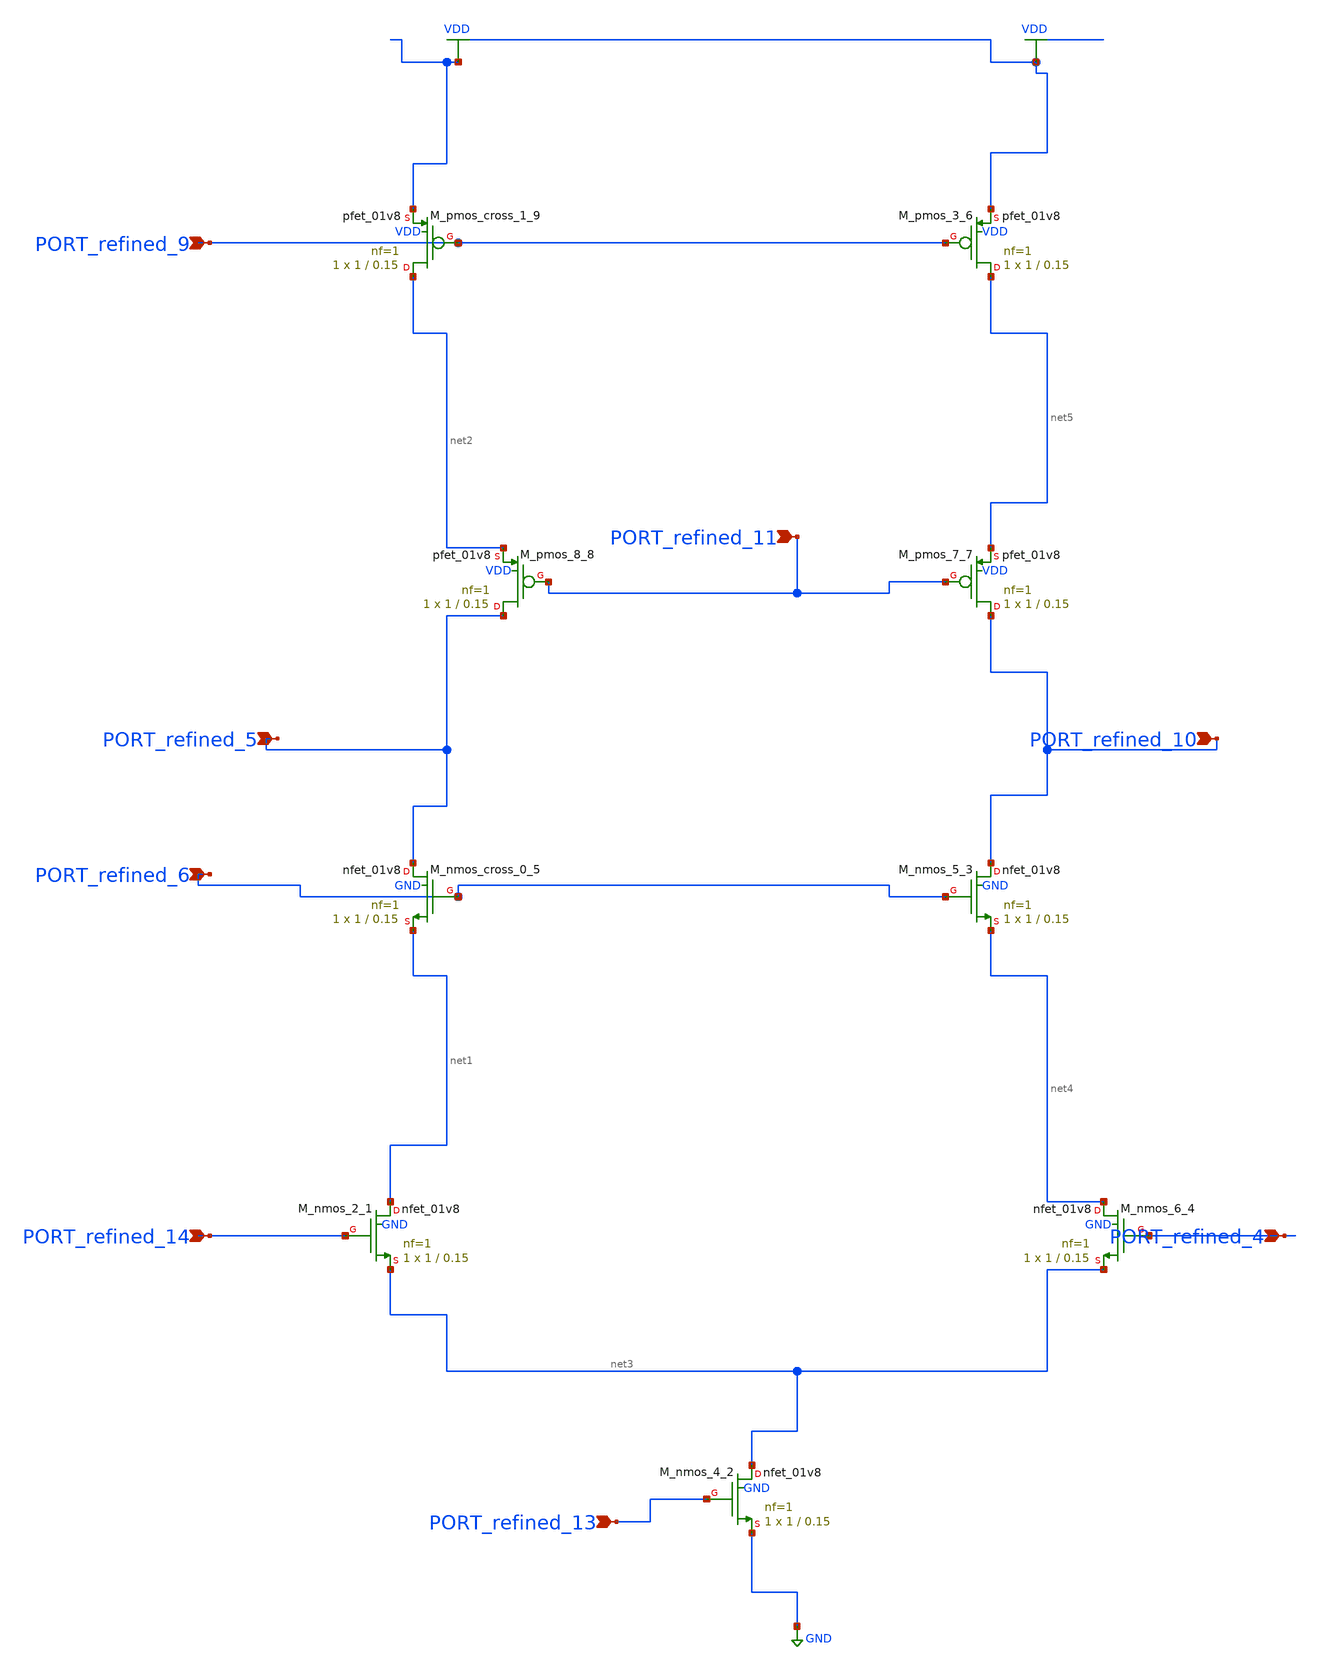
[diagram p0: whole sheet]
** sch_path: schematics/AMSNet/753.sch
**.subckt 753 PORT_refined_13 PORT_refined_4 PORT_refined_6 PORT_refined_11 PORT_refined_10
*+ PORT_refined_14 PORT_refined_5 PORT_refined_9
*.ipin PORT_refined_13
*.ipin PORT_refined_4
*.ipin PORT_refined_6
*.ipin PORT_refined_11
*.ipin PORT_refined_10
*.ipin PORT_refined_14
*.ipin PORT_refined_5
*.ipin PORT_refined_9
XM_nmos_2_1 net1 PORT_refined_14 net3 GND sky130_fd_pr__nfet_01v8 L=0.15 W=1 nf=1 ad='int((1 + 1)/2) * 1 / 1 * 0.29'
+ as='int((1 + 2)/2) * 1 / 1 * 0.29' pd='2*int((1 + 1)/2) * (1 / 1 + 0.29)' ps='2*int((1 + 2)/2) * (1 / 1 + 0.29)'
+ nrd='0.29 / 1 ' nrs='0.29 / 1 ' sa=0 sb=0 sd=0 mult=1 m=1
XM_nmos_4_2 net3 PORT_refined_13 GND GND sky130_fd_pr__nfet_01v8 L=0.15 W=1 nf=1 ad='int((1 + 1)/2) * 1 / 1 * 0.29'
+ as='int((1 + 2)/2) * 1 / 1 * 0.29' pd='2*int((1 + 1)/2) * (1 / 1 + 0.29)' ps='2*int((1 + 2)/2) * (1 / 1 + 0.29)'
+ nrd='0.29 / 1 ' nrs='0.29 / 1 ' sa=0 sb=0 sd=0 mult=1 m=1
XM_nmos_5_3 PORT_refined_10 PORT_refined_6 net4 GND sky130_fd_pr__nfet_01v8 L=0.15 W=1 nf=1 ad='int((1 + 1)/2) * 1 / 1 * 0.29'
+ as='int((1 + 2)/2) * 1 / 1 * 0.29' pd='2*int((1 + 1)/2) * (1 / 1 + 0.29)' ps='2*int((1 + 2)/2) * (1 / 1 + 0.29)'
+ nrd='0.29 / 1 ' nrs='0.29 / 1 ' sa=0 sb=0 sd=0 mult=1 m=1
XM_nmos_6_4 net4 PORT_refined_4 net3 GND sky130_fd_pr__nfet_01v8 L=0.15 W=1 nf=1 ad='int((1 + 1)/2) * 1 / 1 * 0.29'
+ as='int((1 + 2)/2) * 1 / 1 * 0.29' pd='2*int((1 + 1)/2) * (1 / 1 + 0.29)' ps='2*int((1 + 2)/2) * (1 / 1 + 0.29)'
+ nrd='0.29 / 1 ' nrs='0.29 / 1 ' sa=0 sb=0 sd=0 mult=1 m=1
XM_nmos_cross_0_5 PORT_refined_5 PORT_refined_6 net1 GND sky130_fd_pr__nfet_01v8 L=0.15 W=1 nf=1 ad='int((1 + 1)/2) * 1 / 1 * 0.29'
+ as='int((1 + 2)/2) * 1 / 1 * 0.29' pd='2*int((1 + 1)/2) * (1 / 1 + 0.29)' ps='2*int((1 + 2)/2) * (1 / 1 + 0.29)'
+ nrd='0.29 / 1 ' nrs='0.29 / 1 ' sa=0 sb=0 sd=0 mult=1 m=1
XM_pmos_3_6 net5 PORT_refined_9 VDD VDD sky130_fd_pr__pfet_01v8 L=0.15 W=1 nf=1 ad='int((1 + 1)/2) * 1 / 1 * 0.29'
+ as='int((1 + 2)/2) * 1 / 1 * 0.29' pd='2*int((1 + 1)/2) * (1 / 1 + 0.29)' ps='2*int((1 + 2)/2) * (1 / 1 + 0.29)'
+ nrd='0.29 / 1 ' nrs='0.29 / 1 ' sa=0 sb=0 sd=0 mult=1 m=1
XM_pmos_7_7 PORT_refined_10 PORT_refined_11 net5 VDD sky130_fd_pr__pfet_01v8 L=0.15 W=1 nf=1 ad='int((1 + 1)/2) * 1 / 1 * 0.29'
+ as='int((1 + 2)/2) * 1 / 1 * 0.29' pd='2*int((1 + 1)/2) * (1 / 1 + 0.29)' ps='2*int((1 + 2)/2) * (1 / 1 + 0.29)'
+ nrd='0.29 / 1 ' nrs='0.29 / 1 ' sa=0 sb=0 sd=0 mult=1 m=1
XM_pmos_8_8 PORT_refined_5 PORT_refined_11 net2 VDD sky130_fd_pr__pfet_01v8 L=0.15 W=1 nf=1 ad='int((1 + 1)/2) * 1 / 1 * 0.29'
+ as='int((1 + 2)/2) * 1 / 1 * 0.29' pd='2*int((1 + 1)/2) * (1 / 1 + 0.29)' ps='2*int((1 + 2)/2) * (1 / 1 + 0.29)'
+ nrd='0.29 / 1 ' nrs='0.29 / 1 ' sa=0 sb=0 sd=0 mult=1 m=1
XM_pmos_cross_1_9 net2 PORT_refined_9 VDD VDD sky130_fd_pr__pfet_01v8 L=0.15 W=1 nf=1 ad='int((1 + 1)/2) * 1 / 1 * 0.29'
+ as='int((1 + 2)/2) * 1 / 1 * 0.29' pd='2*int((1 + 1)/2) * (1 / 1 + 0.29)' ps='2*int((1 + 2)/2) * (1 / 1 + 0.29)'
+ nrd='0.29 / 1 ' nrs='0.29 / 1 ' sa=0 sb=0 sd=0 mult=1 m=1
**.ends
.GLOBAL GND
.GLOBAL VDD
.end
